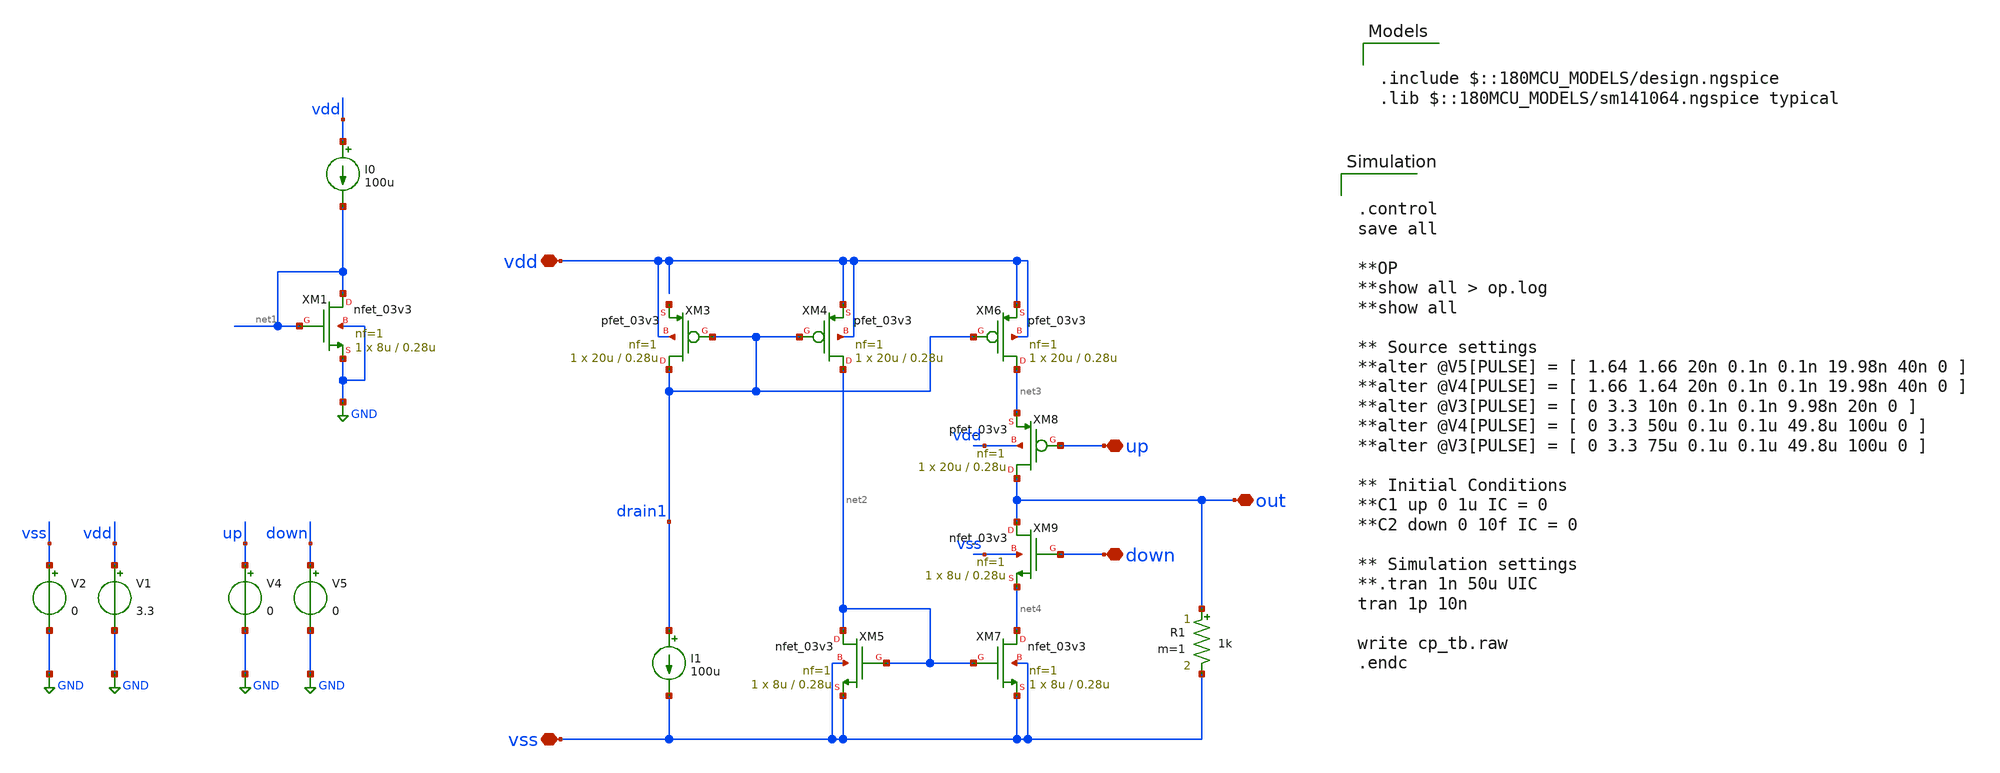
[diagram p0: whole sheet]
** sch_path: designs/cp_tb.sch
**.subckt cp_tb vdd vss up down out
*.iopin vdd
*.iopin vss
*.iopin up
*.iopin down
*.iopin out
V1 vdd GND 3.3
V2 vss GND 0
V4 up GND 0
V5 down GND 0
XM1 net1 net1 GND GND nfet_03v3 L=0.28u W=8u nf=1 ad='int((nf+1)/2) * W/nf * 0.18u' as='int((nf+2)/2) * W/nf * 0.18u'
+ pd='2*int((nf+1)/2) * (W/nf + 0.18u)' ps='2*int((nf+2)/2) * (W/nf + 0.18u)' nrd='0.18u / W' nrs='0.18u / W'
+ sa=0 sb=0 sd=0 m=1
I0 vdd net1 100u
XM3 drain1 drain1 net5 vdd pfet_03v3 L=0.28u W=20u nf=1 ad='int((nf+1)/2) * W/nf * 0.18u' as='int((nf+2)/2) * W/nf * 0.18u'
+ pd='2*int((nf+1)/2) * (W/nf + 0.18u)' ps='2*int((nf+2)/2) * (W/nf + 0.18u)' nrd='0.18u / W' nrs='0.18u / W'
+ sa=0 sb=0 sd=0 m=1
XM4 net2 drain1 vdd vdd pfet_03v3 L=0.28u W=20u nf=1 ad='int((nf+1)/2) * W/nf * 0.18u' as='int((nf+2)/2) * W/nf * 0.18u'
+ pd='2*int((nf+1)/2) * (W/nf + 0.18u)' ps='2*int((nf+2)/2) * (W/nf + 0.18u)' nrd='0.18u / W' nrs='0.18u / W'
+ sa=0 sb=0 sd=0 m=1
XM5 net2 net2 vss vss nfet_03v3 L=0.28u W=8u nf=1 ad='int((nf+1)/2) * W/nf * 0.18u' as='int((nf+2)/2) * W/nf * 0.18u'
+ pd='2*int((nf+1)/2) * (W/nf + 0.18u)' ps='2*int((nf+2)/2) * (W/nf + 0.18u)' nrd='0.18u / W' nrs='0.18u / W'
+ sa=0 sb=0 sd=0 m=1
XM6 net3 drain1 vdd vdd pfet_03v3 L=0.28u W=20u nf=1 ad='int((nf+1)/2) * W/nf * 0.18u' as='int((nf+2)/2) * W/nf * 0.18u'
+ pd='2*int((nf+1)/2) * (W/nf + 0.18u)' ps='2*int((nf+2)/2) * (W/nf + 0.18u)' nrd='0.18u / W' nrs='0.18u / W'
+ sa=0 sb=0 sd=0 m=1
XM7 net4 net2 vss vss nfet_03v3 L=0.28u W=8u nf=1 ad='int((nf+1)/2) * W/nf * 0.18u' as='int((nf+2)/2) * W/nf * 0.18u'
+ pd='2*int((nf+1)/2) * (W/nf + 0.18u)' ps='2*int((nf+2)/2) * (W/nf + 0.18u)' nrd='0.18u / W' nrs='0.18u / W'
+ sa=0 sb=0 sd=0 m=1
XM8 out up net3 vdd pfet_03v3 L=0.28u W=20u nf=1 ad='int((nf+1)/2) * W/nf * 0.18u' as='int((nf+2)/2) * W/nf * 0.18u'
+ pd='2*int((nf+1)/2) * (W/nf + 0.18u)' ps='2*int((nf+2)/2) * (W/nf + 0.18u)' nrd='0.18u / W' nrs='0.18u / W'
+ sa=0 sb=0 sd=0 m=1
XM9 out down net4 vss nfet_03v3 L=0.28u W=8u nf=1 ad='int((nf+1)/2) * W/nf * 0.18u' as='int((nf+2)/2) * W/nf * 0.18u'
+ pd='2*int((nf+1)/2) * (W/nf + 0.18u)' ps='2*int((nf+2)/2) * (W/nf + 0.18u)' nrd='0.18u / W' nrs='0.18u / W'
+ sa=0 sb=0 sd=0 m=1
R1 out vss 1k m=1
I1 drain1 vss 100u
**** begin user architecture code

.include $::180MCU_MODELS/design.ngspice
.lib $::180MCU_MODELS/sm141064.ngspice typical



.control
save all

**OP
**show all > op.log
**show all

** Source settings
**alter @V5[PULSE] = [ 1.64 1.66 20n 0.1n 0.1n 19.98n 40n 0 ]
**alter @V4[PULSE] = [ 1.66 1.64 20n 0.1n 0.1n 19.98n 40n 0 ]
**alter @V3[PULSE] = [ 0 3.3 10n 0.1n 0.1n 9.98n 20n 0 ]
**alter @V4[PULSE] = [ 0 3.3 50u 0.1u 0.1u 49.8u 100u 0 ]
**alter @V3[PULSE] = [ 0 3.3 75u 0.1u 0.1u 49.8u 100u 0 ]

** Initial Conditions
**C1 up 0 1u IC = 0
**C2 down 0 10f IC = 0

** Simulation settings
**.tran 1n 50u UIC
tran 1p 10n

write cp_tb.raw
.endc


**** end user architecture code
**.ends
.GLOBAL GND
.end
